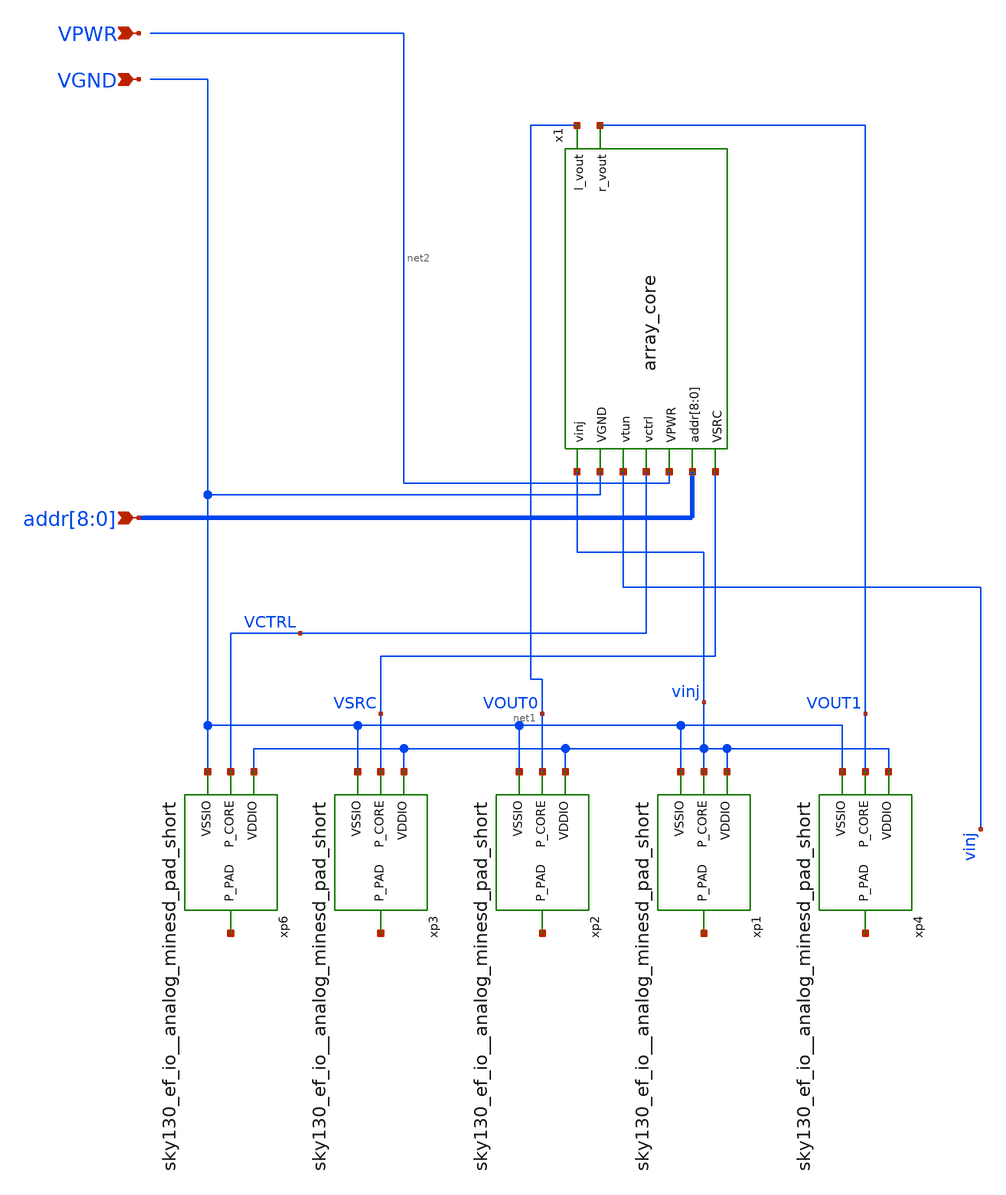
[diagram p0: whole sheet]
** sch_path: xschem/top_fgcaptest.sch
**.subckt top_fgcaptest VPWR VGND
*+ addr[8],addr[7],addr[6],addr[5],addr[4],addr[3],addr[2],addr[1],addr[0]
*.ipin VPWR
*.ipin VGND
*.ipin addr[8],addr[7],addr[6],addr[5],addr[4],addr[3],addr[2],addr[1],addr[0]
x1 vinj net1 vinj VCTRL net2 addr[8] addr[7] addr[6] addr[5] addr[4] addr[3] addr[2] addr[1] addr[0]
+ VOUT0 VOUT1 VSRC array_core
**.ends
.end
